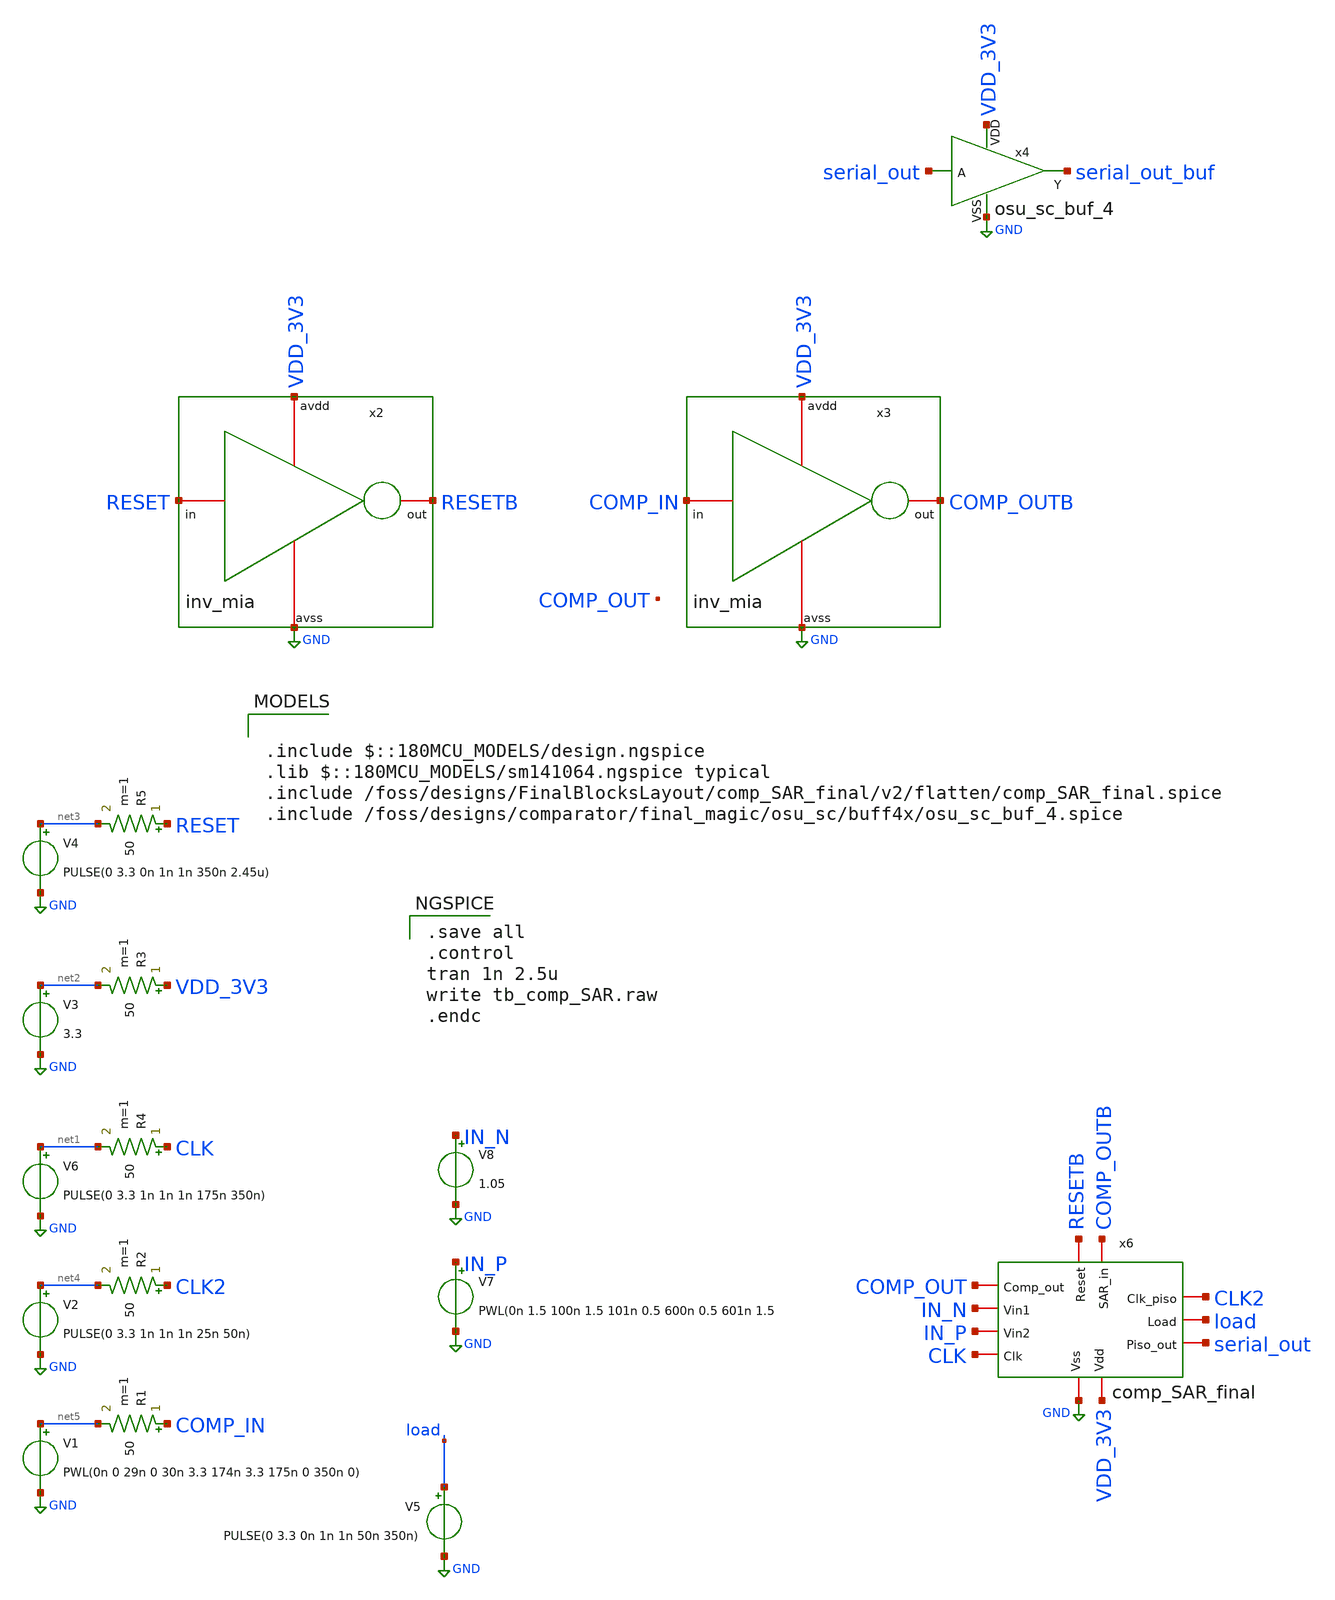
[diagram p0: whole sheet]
** sch_path: designs/FinalBlocksLayout/comp_SAR_final/tb_comp_SAR.sch
**.subckt tb_comp_SAR
V6 net1 GND PULSE(0 3.3 1n 1n 1n 175n 350n)
R4 CLK net1 50 m=1
V3 net2 GND 3.3
R3 VDD_3V3 net2 50 m=1
V4 net3 GND PULSE(0 3.3 0n 1n 1n 350n 2.45u)
R5 RESET net3 50 m=1
x2 VDD_3V3 RESET RESETB GND inv_mia
x3 VDD_3V3 COMP_IN COMP_OUTB GND inv_mia
V2 net4 GND PULSE(0 3.3 1n 1n 1n 25n 50n)
R2 CLK2 net4 50 m=1
V5 load GND PULSE(0 3.3 0n 1n 1n 50n 350n)
x6 CLK2 VDD_3V3 GND load CLK serial_out IN_N IN_P COMP_OUT RESETB COMP_OUTB comp_SAR_final
V7 IN_P GND PWL(0n 1.5 100n 1.5 101n 0.5 600n 0.5 601n 1.5
V8 IN_N GND 1.05
V1 net5 GND PWL(0n 0 29n 0 30n 3.3 174n 3.3 175n 0 350n 0)
R1 COMP_IN net5 50 m=1
x4 VDD_3V3 serial_out serial_out_buf GND osu_sc_buf_4
**** begin user architecture code

.include $::180MCU_MODELS/design.ngspice
.lib $::180MCU_MODELS/sm141064.ngspice typical
.include /foss/designs/FinalBlocksLayout/comp_SAR_final/v2/flatten/comp_SAR_final.spice
.include /foss/designs/comparator/final_magic/osu_sc/buff4x/osu_sc_buf_4.spice


.save all
.control
tran 1n 2.5u
write tb_comp_SAR.raw
.endc

**** end user architecture code
**.ends
.GLOBAL GND
.end
